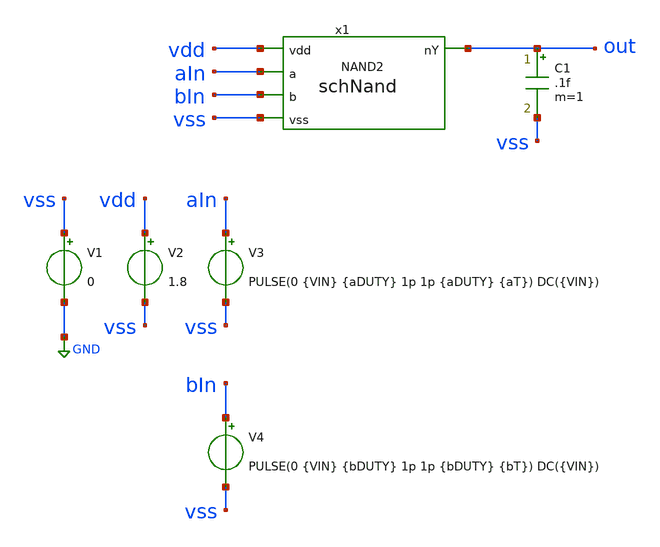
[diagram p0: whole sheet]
** sch_path: eamta2021/sch/nand/tbNand.sch
**.subckt tbNand
x1 vdd out aIn bIn vss schNand
V1 vss GND 0
V2 vdd vss 1.8
V3 aIn vss PULSE(0 {VIN} {aDUTY} 1p 1p {aDUTY} {aT}) DC({VIN})
C1 out vss .1f m=1
V4 bIn vss PULSE(0 {VIN} {bDUTY} 1p 1p {bDUTY} {bT}) DC({VIN})
**** begin user architecture code



* parametros
.param VIN=1.8 aT=100n aDUTY=50n bT=100n bDUTY=50n WN=.450 WP=.90
.options TEMP=27.0

* include corners
.lib /home/eamta/skywater/skywater-pdk/libraries/sky130_fd_pr_ngspice/latest/models/corners/sky130.lib TT

* saves
.save all
**PFETs  @M.x1.xm1.msky130_fd_pr__pfet_01v8[id]  @M.x1.xm1.msky130_fd_pr__pfet_01v8[vds]
*+  @M.x1.xm1.msky130_fd_pr__pfet_01v8[vgs]  @M.x1.xm1.msky130_fd_pr__pfet_01v8[vth]  @M.x1.xm2.msky130_fd_pr__pfet_01v8[id]
*+  @M.x1.xm2.msky130_fd_pr__pfet_01v8[vds]  @M.x1.xm2.msky130_fd_pr__pfet_01v8[vgs]  @M.x1.xm2.msky130_fd_pr__pfet_01v8[vth]
**NFETs  @M.x1.xm3.msky130_fd_pr__nfet_01v8[id]  @M.x1.xm3.msky130_fd_pr__nfet_01v8[vds]
*+  @M.x1.xm3.msky130_fd_pr__nfet_01v8[vgs]  @M.x1.xm3.msky130_fd_pr__nfet_01v8[vth]  @M.x1.xm4.msky130_fd_pr__nfet_01v8[id]
*+  @M.x1.xm4.msky130_fd_pr__nfet_01v8[vds]  @M.x1.xm4.msky130_fd_pr__nfet_01v8[vgs]  @M.x1.xm4.msky130_fd_pr__nfet_01v8[vth]

* SIM
.control
	******************************************************
	*let At=.005ns

	tran 0.005ns 500ns

	setplot tran1
	**comportamiento
	*plot v(aIn) v(bIn)+2 v(out)+4
	**rise/fall
	plot v(out) v(aIn) .18 1.62 xlimit 50ns 50.05ns
	plot v(out) v(aIn) .18 1.62 xlimit 100ns 100.05ns
	**sos inimputable
	*plot tran1.@M.x1.xm1.msky130_fd_pr__nfet_01v8[vds]
	*plot tran1.@M.x1.xm1.msky130_fd_pr__nfet_01v8[id] tran1.@M.x1.xm2.msky130_fd_pr__pfet_01v8[id]

	*set filetype=ascii
	*write simInvTran.raw
	*reset
	******************************************************
	*alterparam bDUTY=100n
	*dc V3 0 1.8 0.01
	*alterparam aDUTY=100n
	*dc V4 0 1.8 0.01
	*dc V3 0 1.8 0.01 V4 0 1.8 0.01

	*setplot dc1
	*plot dc1.out vs dc1.aIn dc2.out vs dc2.bIn dc3.out vs dc3.aIn
	*plot @M.x1.xm1.msky130_fd_pr__nfet_01v8[id]
	*plot @M.x1.xm1.msky130_fd_pr__nfet_01v8[vd]

	*set filetype=ascii
	*write simInvDc.raw
	*reset
	******************************************************
	op

	set filetype=ascii
	write simInvOp.raw

***********************************************************
	*analisis cuasi parametrico
	*let actParam=1ps
	*let topParam=100ps
	*let detlaParam=10ps

	*foreach x 1ps 10ps 20ps 30ps 40ps 50ps
	*	alterparam THL=$x
	*	tran .01ns .1us
	*	let actParam=actParam+deltaParam
	*	print $x
	*end

	*plot tran1.out tran2.out tran3.out tran4.out tran5.out tran6.out tran7.out tran8.out tran9.out

	print all
.endc

.end


**** end user architecture code
**.ends

* expanding   symbol:  nand/schNand.sym # of pins=5
** sym_path: eamta2021/sch/nand/schNand.sym
** sch_path: eamta2021/sch/nand/schNand.sch
.subckt schNand vdd nY a b vss
*.ipin vdd
*.ipin vss
*.ipin a
*.ipin b
*.opin nY
XM1 nY b vdd vdd sky130_fd_pr__pfet_01v8 L=0.15 W={WP} nf=1 ad='int((nf+1)/2) * W/nf * 0.29' as='int((nf+2)/2) * W/nf * 0.29'
+ pd='2*int((nf+1)/2) * (W/nf + 0.29)' ps='2*int((nf+2)/2) * (W/nf + 0.29)' nrd='0.29 / W' nrs='0.29 / W'
+ sa=0 sb=0 sd=0 mult=1 m=1
XM2 nY a vdd vdd sky130_fd_pr__pfet_01v8 L=0.15 W={WP} nf=1 ad='int((nf+1)/2) * W/nf * 0.29' as='int((nf+2)/2) * W/nf * 0.29'
+ pd='2*int((nf+1)/2) * (W/nf + 0.29)' ps='2*int((nf+2)/2) * (W/nf + 0.29)' nrd='0.29 / W' nrs='0.29 / W'
+ sa=0 sb=0 sd=0 mult=1 m=1
XM3 nY a net1 vss sky130_fd_pr__nfet_01v8 L=0.15 W={WN} nf=1 ad='int((nf+1)/2) * W/nf * 0.29' as='int((nf+2)/2) * W/nf * 0.29'
+ pd='2*int((nf+1)/2) * (W/nf + 0.29)' ps='2*int((nf+2)/2) * (W/nf + 0.29)' nrd='0.29 / W' nrs='0.29 / W'
+ sa=0 sb=0 sd=0 mult=1 m=1
XM4 net1 b vss vss sky130_fd_pr__nfet_01v8 L=0.15 W={WN} nf=1 ad='int((nf+1)/2) * W/nf * 0.29' as='int((nf+2)/2) * W/nf * 0.29'
+ pd='2*int((nf+1)/2) * (W/nf + 0.29)' ps='2*int((nf+2)/2) * (W/nf + 0.29)' nrd='0.29 / W' nrs='0.29 / W'
+ sa=0 sb=0 sd=0 mult=1 m=1
.ends

.GLOBAL GND
.end
